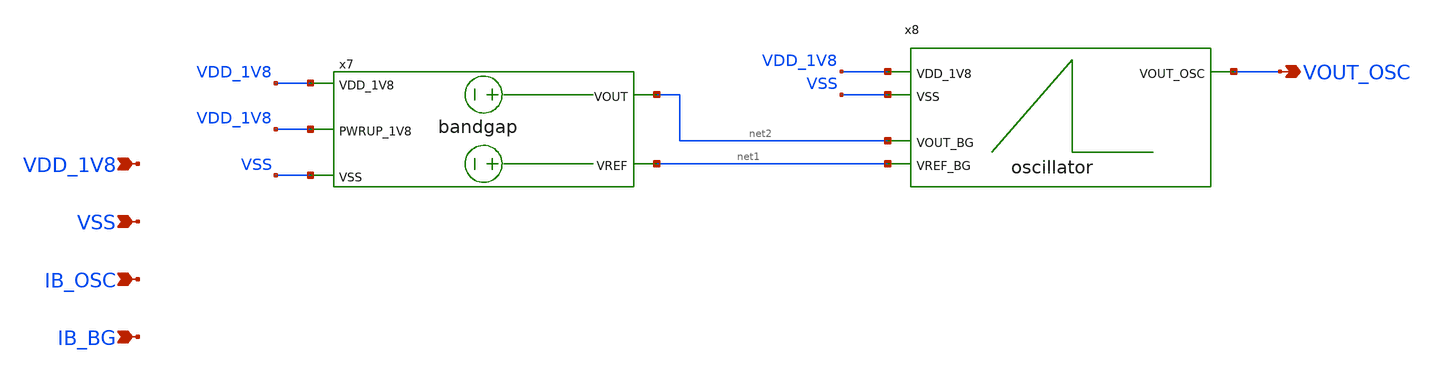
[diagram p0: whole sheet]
** sch_path: design/LELO_GR01_SKY130A/oscillator_tb.sch
**.subckt oscillator_tb VSS VDD_1V8 IB_OSC IB_BG VOUT_OSC
*.ipin VSS
*.ipin VDD_1V8
*.ipin IB_OSC
*.ipin IB_BG
*.opin VOUT_OSC
x7 net2 net1 VDD_1V8 VDD_1V8 VSS bandgap
x8 VOUT_OSC VDD_1V8 VSS net2 net1 oscillator
**.ends
.end
